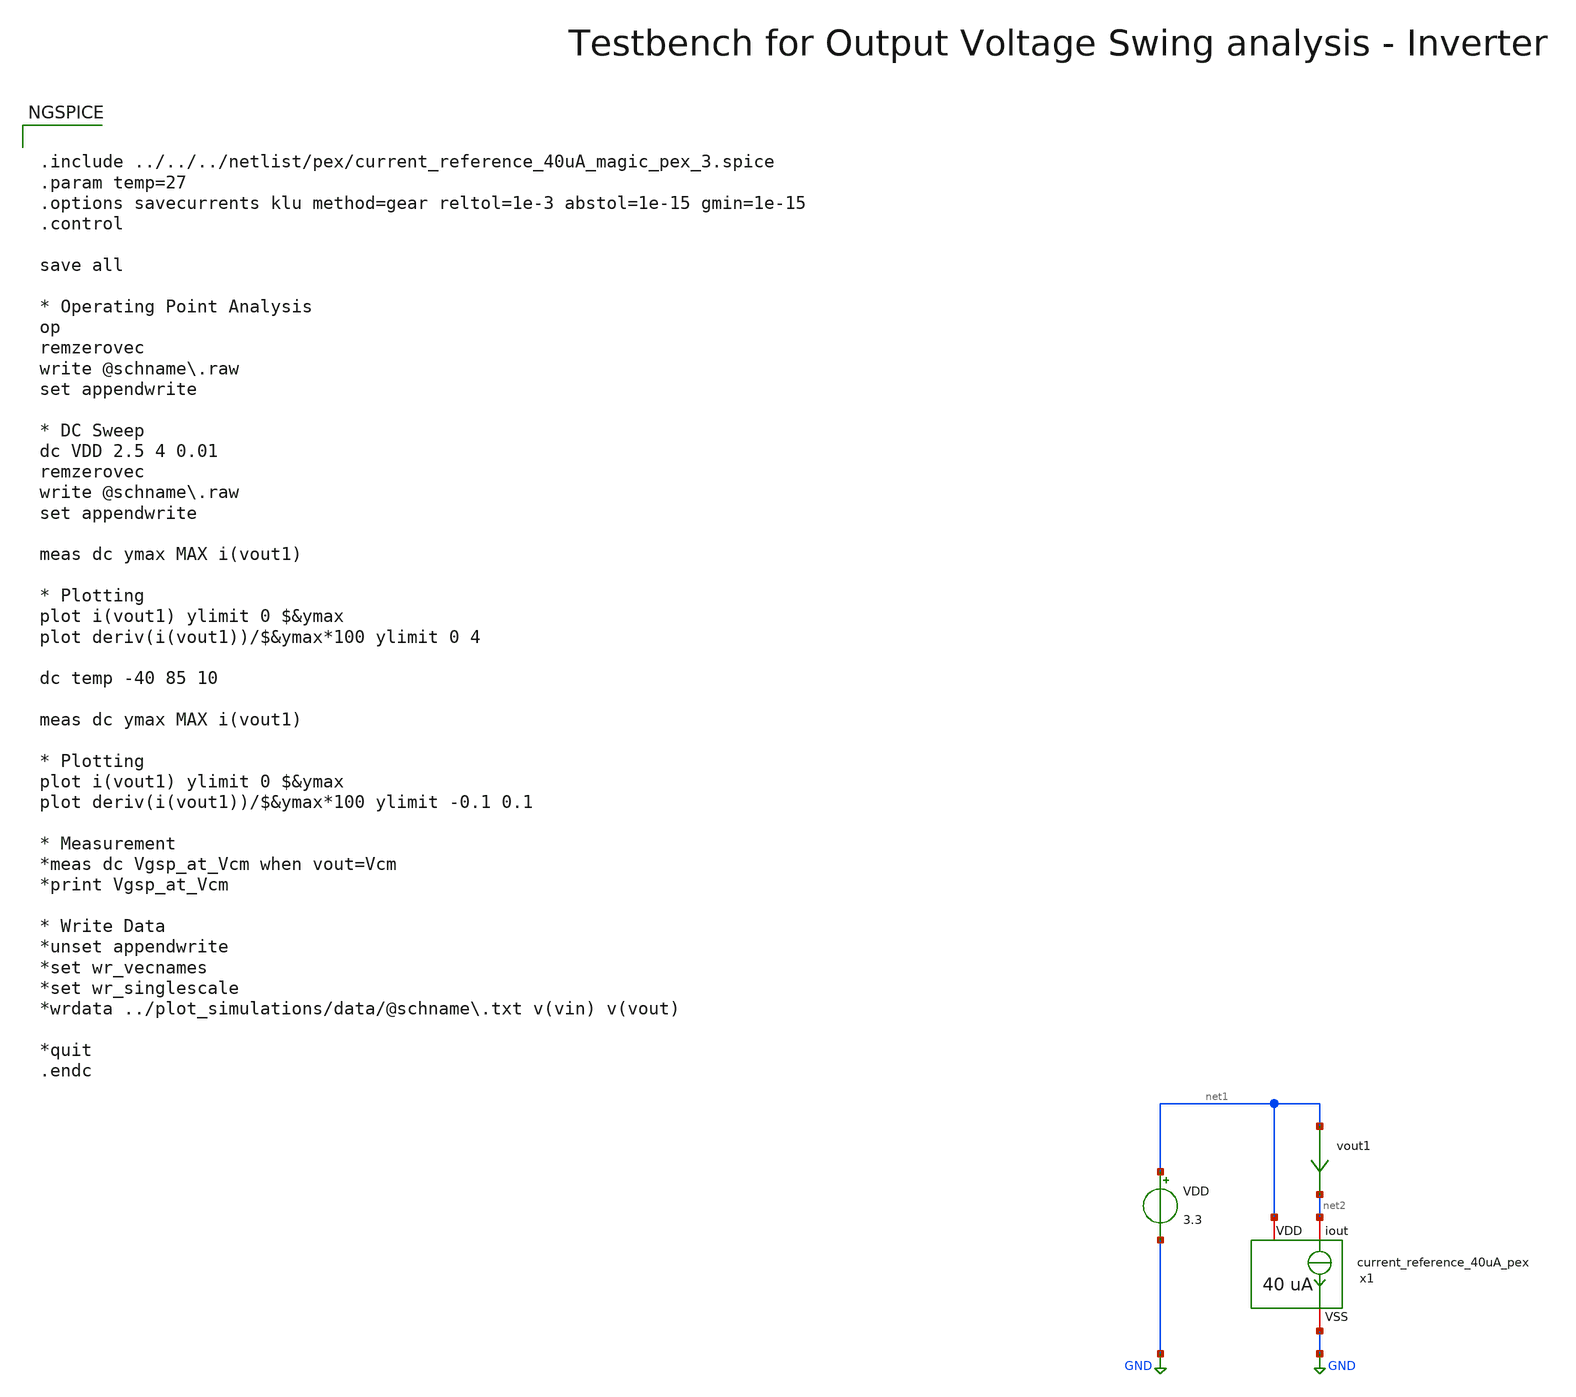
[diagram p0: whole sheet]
** sch_path: macros/heichips26_vcr/macros/switched_capacitor/testbenches/xschem/tb_current_reference_pex_dc.sch
**.subckt tb_current_reference_pex_dc
VDD net1 GND 3.3
vout1 net1 net2 0
.save i(vout1)
x1 net1 net2 GND current_reference_40uA_pex
**** begin user architecture code


.include ../../../netlist/pex/current_reference_40uA_magic_pex_3.spice
.param temp=27
.options savecurrents klu method=gear reltol=1e-3 abstol=1e-15 gmin=1e-15
.control

save all

* Operating Point Analysis
op
remzerovec
write @schname\.raw
set appendwrite

* DC Sweep
dc VDD 2.5 4 0.01
remzerovec
write @schname\.raw
set appendwrite

meas dc ymax MAX i(vout1)

* Plotting
plot i(vout1) ylimit 0 $&ymax
plot deriv(i(vout1))/$&ymax*100 ylimit 0 4

dc temp -40 85 10

meas dc ymax MAX i(vout1)

* Plotting
plot i(vout1) ylimit 0 $&ymax
plot deriv(i(vout1))/$&ymax*100 ylimit -0.1 0.1

* Measurement
*meas dc Vgsp_at_Vcm when vout=Vcm
*print Vgsp_at_Vcm

* Write Data
*unset appendwrite
*set wr_vecnames
*set wr_singlescale
*wrdata ../plot_simulations/data/@schname\.txt v(vin) v(vout)

*quit
.endc



.lib cornerMOSlv.lib mos_tt
.lib cornerMOShv.lib mos_tt
.lib cornerRES.lib res_typ
.lib cornerDIO.lib dio_tt

**** end user architecture code
**.ends
.GLOBAL GND
.end
